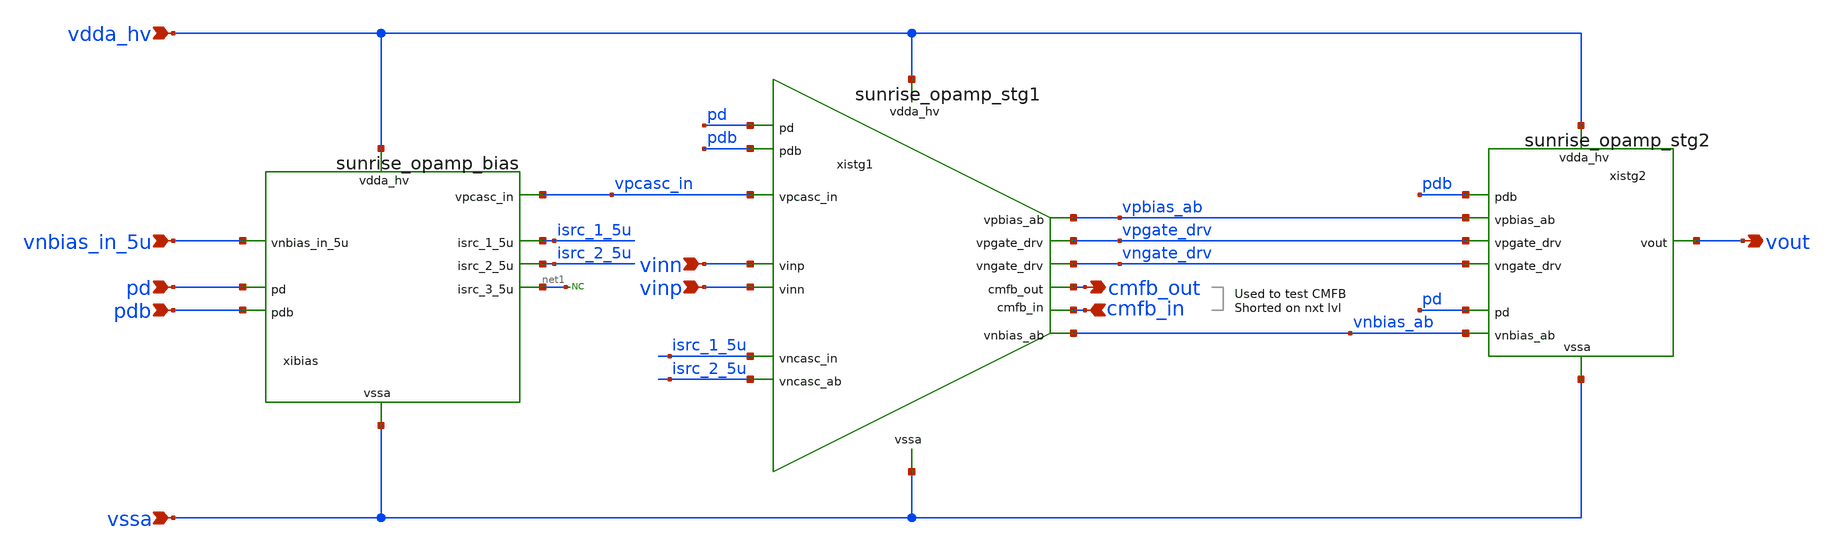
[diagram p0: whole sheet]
** sch_path: Schematics_Layout/sunrise_opamp_cmfb_prb/sunrise_opamp_cmfb_prb.sch
**.subckt sunrise_opamp_cmfb_prb vinp vinn pd pdb vnbias_in_5u vssa vdda_hv vout cmfb_in cmfb_out
*.ipin vinp
*.ipin vinn
*.ipin pd
*.ipin pdb
*.ipin vnbias_in_5u
*.ipin vssa
*.ipin vdda_hv
*.opin vout
*.ipin cmfb_in
*.opin cmfb_out
xistg2 vdda_hv pdb vpgate_drv vout vngate_drv pd vssa vpbias_ab vnbias_ab sunrise_opamp_stg2
xibias vdda_hv pdb vnbias_in_5u isrc_1_5u vpcasc_in pd vssa isrc_2_5u net1 sunrise_opamp_bias
xistg1 vdda_hv pdb vpcasc_in vpgate_drv vinp vinn pd vngate_drv cmfb_out cmfb_in isrc_1_5u vssa
+ vpbias_ab isrc_2_5u vnbias_ab sunrise_opamp_stg1
* noconn #net1
**.ends
.end
